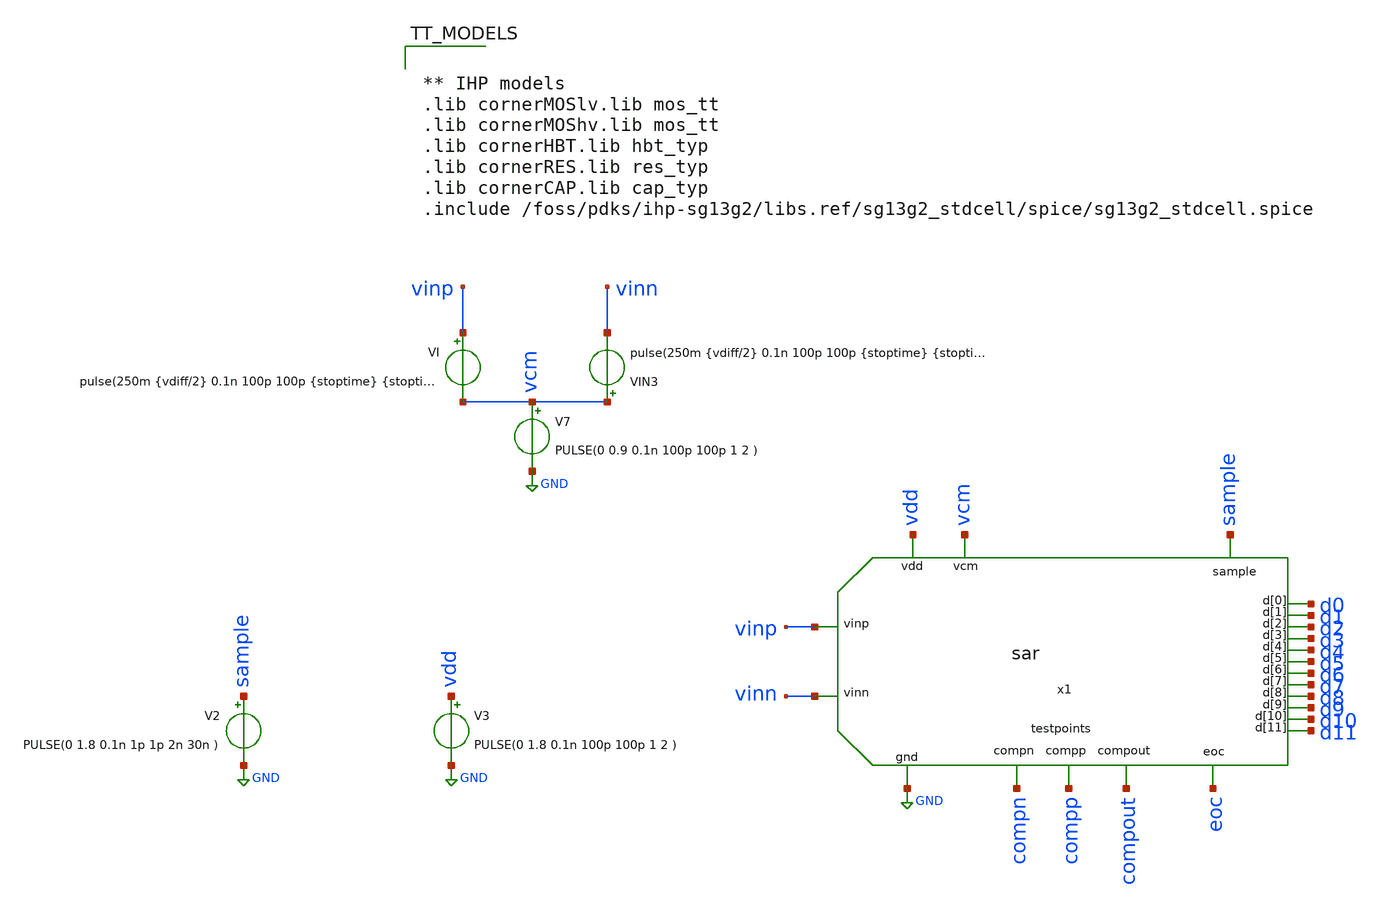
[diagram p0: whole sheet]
** sch_path: xschem/SAR_ADC/testbench/tb_sar_adc.sch
**.subckt tb_sar_adc
x1 vinp sample vinn GND vdd compn compp compout eoc d9 d7 d0 d11 d3 d4 d2 d1 d8 d6 d5 d10 vcm sar
VI vinp vcm pulse(250m {vdiff/2} 0.1n 100p 100p {stoptime} {stoptime+1} 1)
VIN3 vcm vinn pulse(250m {vdiff/2} 0.1n 100p 100p {stoptime} {stoptime+1} 1)
V2 sample GND PULSE(0 1.8 0.1n 1p 1p 2n 30n )
V3 vdd GND PULSE(0 1.8 0.1n 100p 100p 1 2 )
V7 vcm GND PULSE(0 0.9 0.1n 100p 100p 1 2 )
**** begin user architecture code


.param periodclk=1n
.param periodconv=20n
.param stoptime=1*periodconv
.param ro = 300

.param W_P = 0.5u
.param L_P = 0.13u
.param W_N = 0.5u
.param L_N = 0.13u

.param vdiff = 1.796484

.options klu method=gear reltol=1e-2 abstol=1e-15 gmin=1e-15


.tran {0.005*periodclk} {stoptime}

.control

run
set hcopydevtype = svg
set color0 = white
set color1 = black

meas tran eoc_t WHEN eoc=1.7 CROSS=LAST
meas tran soc_t WHEN sample=1.6 FALL=1
meas tran i_rms RMS i(V3) from=soc_t to=eoc_t

let vin = vinp-vinn
let vin_comp = compp-compn
let resultado = {(((V(d11)/1.8)*2048 + (V(d10)/1.8)*1024 + (V(d9)/1.8)*512 + (V(d8)/1.8)*256 + (V(d7)/1.8)*128 + (V(d6)/1.8)*64 + (V(d5)/1.8)*32 + (V(d4)/1.8)*16 + (V(d3)/1.8)*8 + (V(d2)/1.8)*4 + (V(d1)/1.8)*2 + (V(d0)/1.8)) - 2048) * 1.8/2048}
let resultado2 = {((((0-V(d11))/1.8)*2048 + (V(d10)/1.8)*1024 + (V(d9)/1.8)*512 + (V(d8)/1.8)*256 + (V(d7)/1.8)*128 + (V(d6)/1.8)*64 + (V(d5)/1.8)*32 + (V(d4)/1.8)*16 + (V(d3)/1.8)*8 + (V(d2)/1.8)*4 + (V(d1)/1.8)*2 + (V(d0)/1.8)) + 2048)*1.8/2048}
let clk = x1.comp_clk
let vdd = 1.8
let tiempo_conv = eoc_t-soc_t
let potencia_rms = i_rms*vdd
let energia_conv = potencia_rms*(eoc_t-soc_t)
let energia_bit = energia_conv/12
let a_sample_buf = x1.x2.a_sample
let b_sample_buf = x1.x2.b_sample
let a_sample_n_buf = x1.x2.a_sample_n
let b_sample_n_buf = x1.x2.b_sample_n
let a_sample_nol = x1.x2.a_ctrl
let b_sample_nol = x1.x2.b_ctrl
meas tran resultado_final find resultado WHEN eoc=1.7 CROSS=LAST
let error = vin-resultado_final


plot compp compn {compout + 4}
plot {d0} {d1 + 4} {d2 + 8} {d3 + 12} {d4 + 16} {d5 + 20} {d6 + 24} {d7 + 28} {d8 + 32} {d9 + 36} {d10 + 40}
+ {d11 + 44} {clk + 50} {compout + 55} {eoc + 60}  {vin_comp - 2}
plot compp-compn x1.clk compout
*plot sample eoc x1.x3.start
plot resultado sample eoc vin
plot resultado sample eoc vin

print i_rms potencia_rms energia_conv energia_bit > ./../../out/consumos_conversion.txt
print vin resultado_final error tiempo_conv ./../../out/error_ejemplo.txt

hardcopy ./../../img/salidas_SAR.svg {d0} {d1 + 4} {d2 + 8} {d3 + 12} {d4 + 16} {d5 + 20} {d6 + 24} {d7 + 28}
+ {d8 + 32} {d9 + 36} {d10 + 40} {d11 + 44} {clk + 50} {compout + 55} {eoc + 60}  {vin_comp - 2} title
+ 'Salidas SAR'
hardcopy ./../../img/conversion_ejemplo.svg resultado sample eoc vin title 'Conversion de Vin=V1.796484'
*hardcopy ./../../img/conversion2_ejemplo.svg resultado2 sample eoc vin
*hardcopy ./../../img/nol_formas_de_onda.svg sample a_sample_nol+2 b_sample_nol+4 a_sample_buf+2 b_sample_buf+4
*+ xlimit 0 4n title 'Señales de Non-Overlap'
*hardcopy ./../../img/nol_salidas.svg sample a_sample_buf+2 a_sample_n_buf+2 b_sample_buf+4 b_sample_n_buf+4
*+ xlimit 0 4n title 'Salidas del Non-Overlap'
*hardcopy ./../../img/conversion_comparador.svg vin_comp compout clk*.5 title 'Ejemplo convesion comparador'



*wrdata adc_signals.csv time V(d0) V(d1) V(d2) V(d3) V(d4) V(d5) V(d6) V(d7) V(d8) V(d9) V(d10)
*+ V(d11) vinp vinn eoc sample compout compp compn x1.comp_clk
*write adc_signals.raw time V(d0) V(d1) V(d2) V(d3) V(d4) V(d5) V(d6) V(d7) V(d8) V(d9) V(d10)
*+ V(d11) vinp vinn eoc sample compout compp compn x1.comp_clk
*quit
.endc




** IHP models
.lib cornerMOSlv.lib mos_tt
.lib cornerMOShv.lib mos_tt
.lib cornerHBT.lib hbt_typ
.lib cornerRES.lib res_typ
.lib cornerCAP.lib cap_typ
.include /foss/pdks/ihp-sg13g2/libs.ref/sg13g2_stdcell/spice/sg13g2_stdcell.spice


**** end user architecture code
**.ends
.GLOBAL GND
.end
